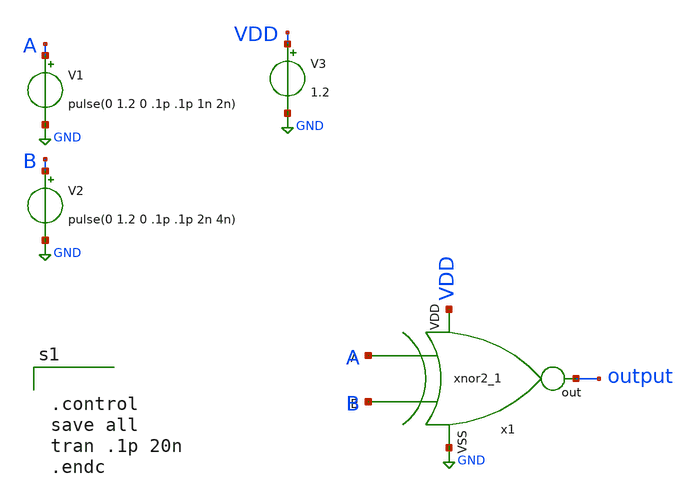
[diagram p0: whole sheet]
** sch_path: xnor2/xnor2_tb.sch
**.subckt xnor2_tb
x1 A B VDD output GND xnor2
V1 A GND pulse(0 1.2 0 .1p .1p 1n 2n)
V2 B GND pulse(0 1.2 0 .1p .1p 2n 4n)
V3 VDD GND 1.2
**** begin user architecture code

** opencircuitdesign pdks install
.lib $::SKYWATER_MODELS/sky130.lib.spice tt




.control
save all
tran .1p 20n
.endc

**** end user architecture code
**.ends
.GLOBAL GND
.end
